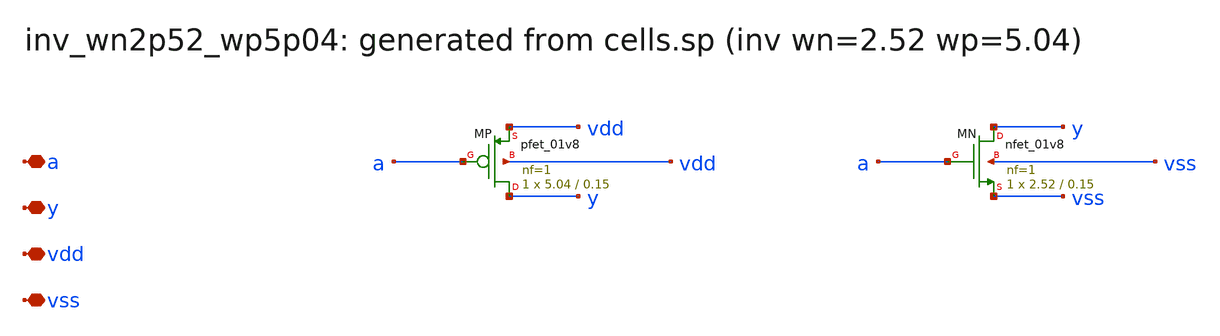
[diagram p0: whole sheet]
** sch_path: sram/xschem/inv_wn2p52_wp5p04.sch
**.subckt inv_wn2p52_wp5p04 a y vdd vss
*.iopin a
*.iopin y
*.iopin vdd
*.iopin vss
XMP y a vdd vdd sky130_fd_pr__pfet_01v8 L=0.15 W=5.04 nf=1 ad='int((nf+1)/2) * W/nf * 0.29' as='int((nf+2)/2) * W/nf * 0.29'
+ pd='2*int((nf+1)/2) * (W/nf + 0.29)' ps='2*int((nf+2)/2) * (W/nf + 0.29)' nrd='0.29 / W' nrs='0.29 / W'
+ sa=0 sb=0 sd=0 mult=1 m=1
XMN y a vss vss sky130_fd_pr__nfet_01v8 L=0.15 W=2.52 nf=1 ad='int((1 + 1)/2) * 2.52 / 1 * 0.29' as='int((1 + 2)/2) * 2.52 / 1 * 0.29'
+ pd='2*int((1 + 1)/2) * (2.52 / 1 + 0.29)' ps='2*int((1 + 2)/2) * (2.52 / 1 + 0.29)' nrd='0.29 / 2.52 '
+ nrs='0.29 / 2.52 ' sa=0 sb=0 sd=0 mult=1 m=1
**.ends
.end
